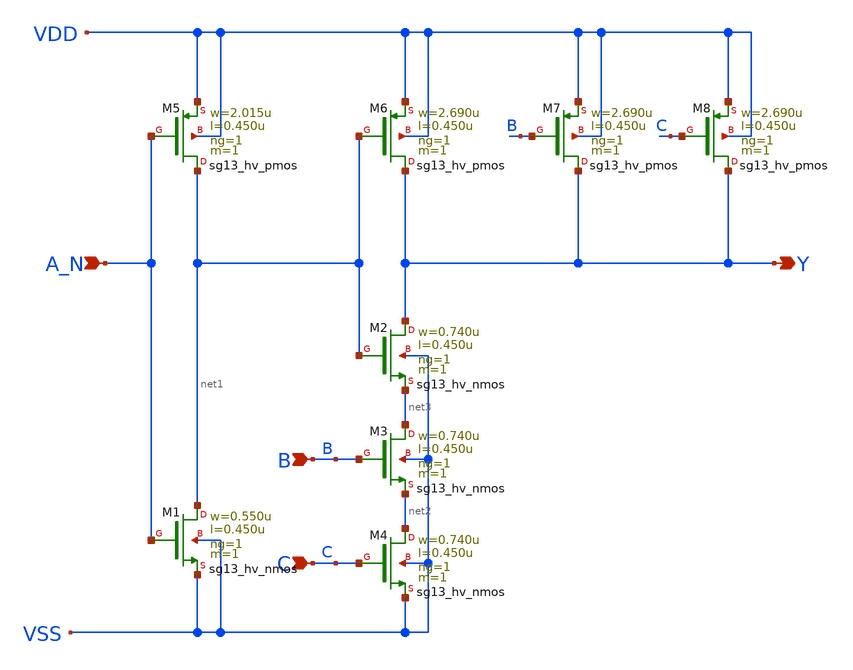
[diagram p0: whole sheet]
** sch_path: ihp-sg13g2/libs.ref/sg13g2_stdcell_hv/sch/xschem/sg13g2_hv_nand3b_1.sch
* Copyright 2023 IHP PDK Authors
* Licensed under the Apache License, Version 2.0 (the "License");
* you may not use this file except in compliance with the License.
* You may obtain a copy of the License at
* https://www.apache.org/licenses/LICENSE-2.0
* Unless required by applicable law or agreed to in writing, software
* distributed under the License is distributed on an "AS IS" BASIS,
* WITHOUT WARRANTIES OR CONDITIONS OF ANY KIND, either express or implied.
* See the License for the specific language governing permissions and
* limitations under the License.
**.subckt sg13g2_hv_nand3b_1 A_N B C Y
*.ipin A_N
*.ipin B
*.ipin C
*.opin Y
XM1 net1 A_N VSS VSS sg13_hv_nmos w=0.550u l=0.450u ng=1 m=1 mm_ok=1
XM2 Y net1 net3 VSS sg13_hv_nmos w=0.740u l=0.450u ng=1 m=1 mm_ok=1
XM3 net3 B net2 VSS sg13_hv_nmos w=0.740u l=0.450u ng=1 m=1 mm_ok=1
XM4 net2 C VSS VSS sg13_hv_nmos w=0.740u l=0.450u ng=1 m=1 mm_ok=1
XM5 net1 A_N VDD VDD sg13_hv_pmos w=2.015u l=0.450u ng=1 m=1 mm_ok=1
XM6 Y net1 VDD VDD sg13_hv_pmos w=2.690u l=0.450u ng=1 m=1 mm_ok=1
XM7 Y B VDD VDD sg13_hv_pmos w=2.690u l=0.450u ng=1 m=1 mm_ok=1
XM8 Y C VDD VDD sg13_hv_pmos w=2.690u l=0.450u ng=1 m=1 mm_ok=1
**.ends
.end
